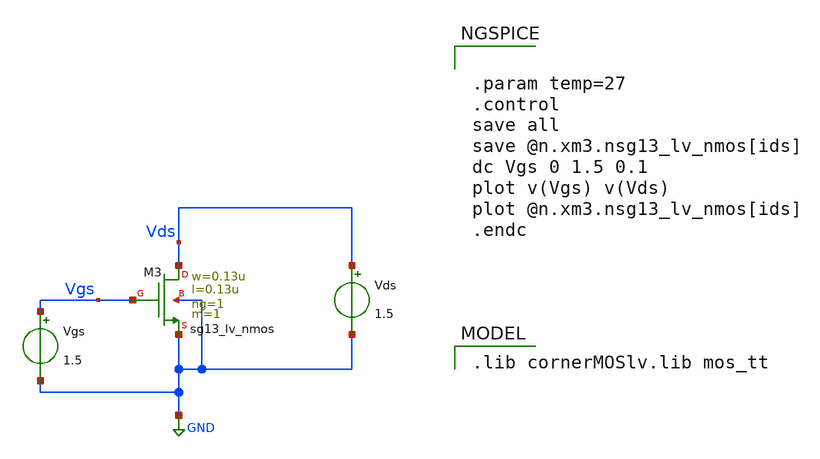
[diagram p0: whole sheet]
** sch_path: xschem/Vth_test.sch
**.subckt Vth_test
XM3 Vds Vgs GND GND sg13_lv_nmos w=0.13u l=0.13u ng=1 m=1 mm_ok=1
Vgs Vgs GND 1.5
Vds Vds GND 1.5
**** begin user architecture code


.param temp=27
.control
save all
save @n.xm3.nsg13_lv_nmos[ids]
dc Vgs 0 1.5 0.1
plot v(Vgs) v(Vds)
plot @n.xm3.nsg13_lv_nmos[ids]
.endc


 .lib cornerMOSlv.lib mos_tt

**** end user architecture code
**.ends
.GLOBAL GND
.end
